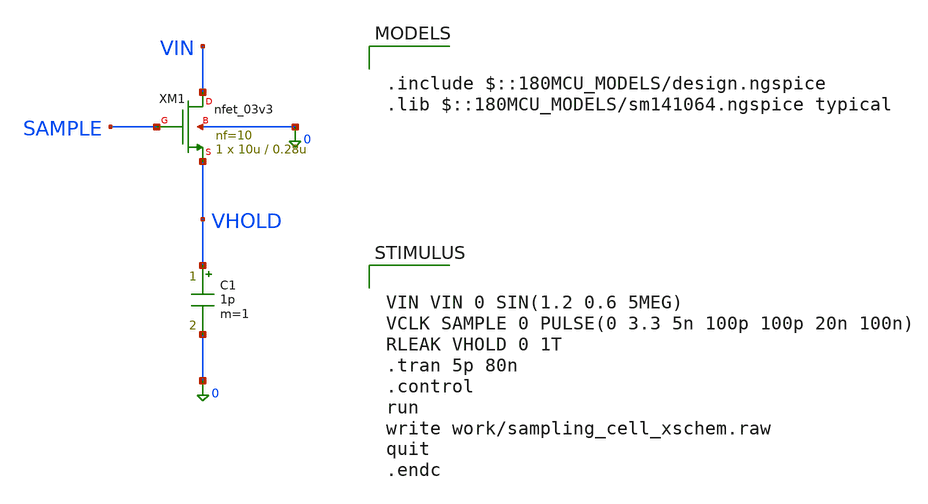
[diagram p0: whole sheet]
** sch_path: simulations/gf180_sampling_cell/sampling_cell.sch
**.subckt sampling_cell
XM1 VIN SAMPLE VHOLD 0 nfet_03v3 L=0.28u W=10u nf=10 ad='int((nf+1)/2) * W/nf * 0.18u' as='int((nf+2)/2) * W/nf * 0.18u'
+ pd='2*int((nf+1)/2) * (W/nf + 0.18u)' ps='2*int((nf+2)/2) * (W/nf + 0.18u)' nrd='0.18u / W' nrs='0.18u / W'
+ sa=0 sb=0 sd=0 m=1
C1 VHOLD 0 1p m=1
**** begin user architecture code

.include $::180MCU_MODELS/design.ngspice
.lib $::180MCU_MODELS/sm141064.ngspice typical



VIN VIN 0 SIN(1.2 0.6 5MEG)
VCLK SAMPLE 0 PULSE(0 3.3 5n 100p 100p 20n 100n)
RLEAK VHOLD 0 1T
.tran 5p 80n
.control
run
write work/sampling_cell_xschem.raw
quit
.endc


**** end user architecture code
**.ends
.end
